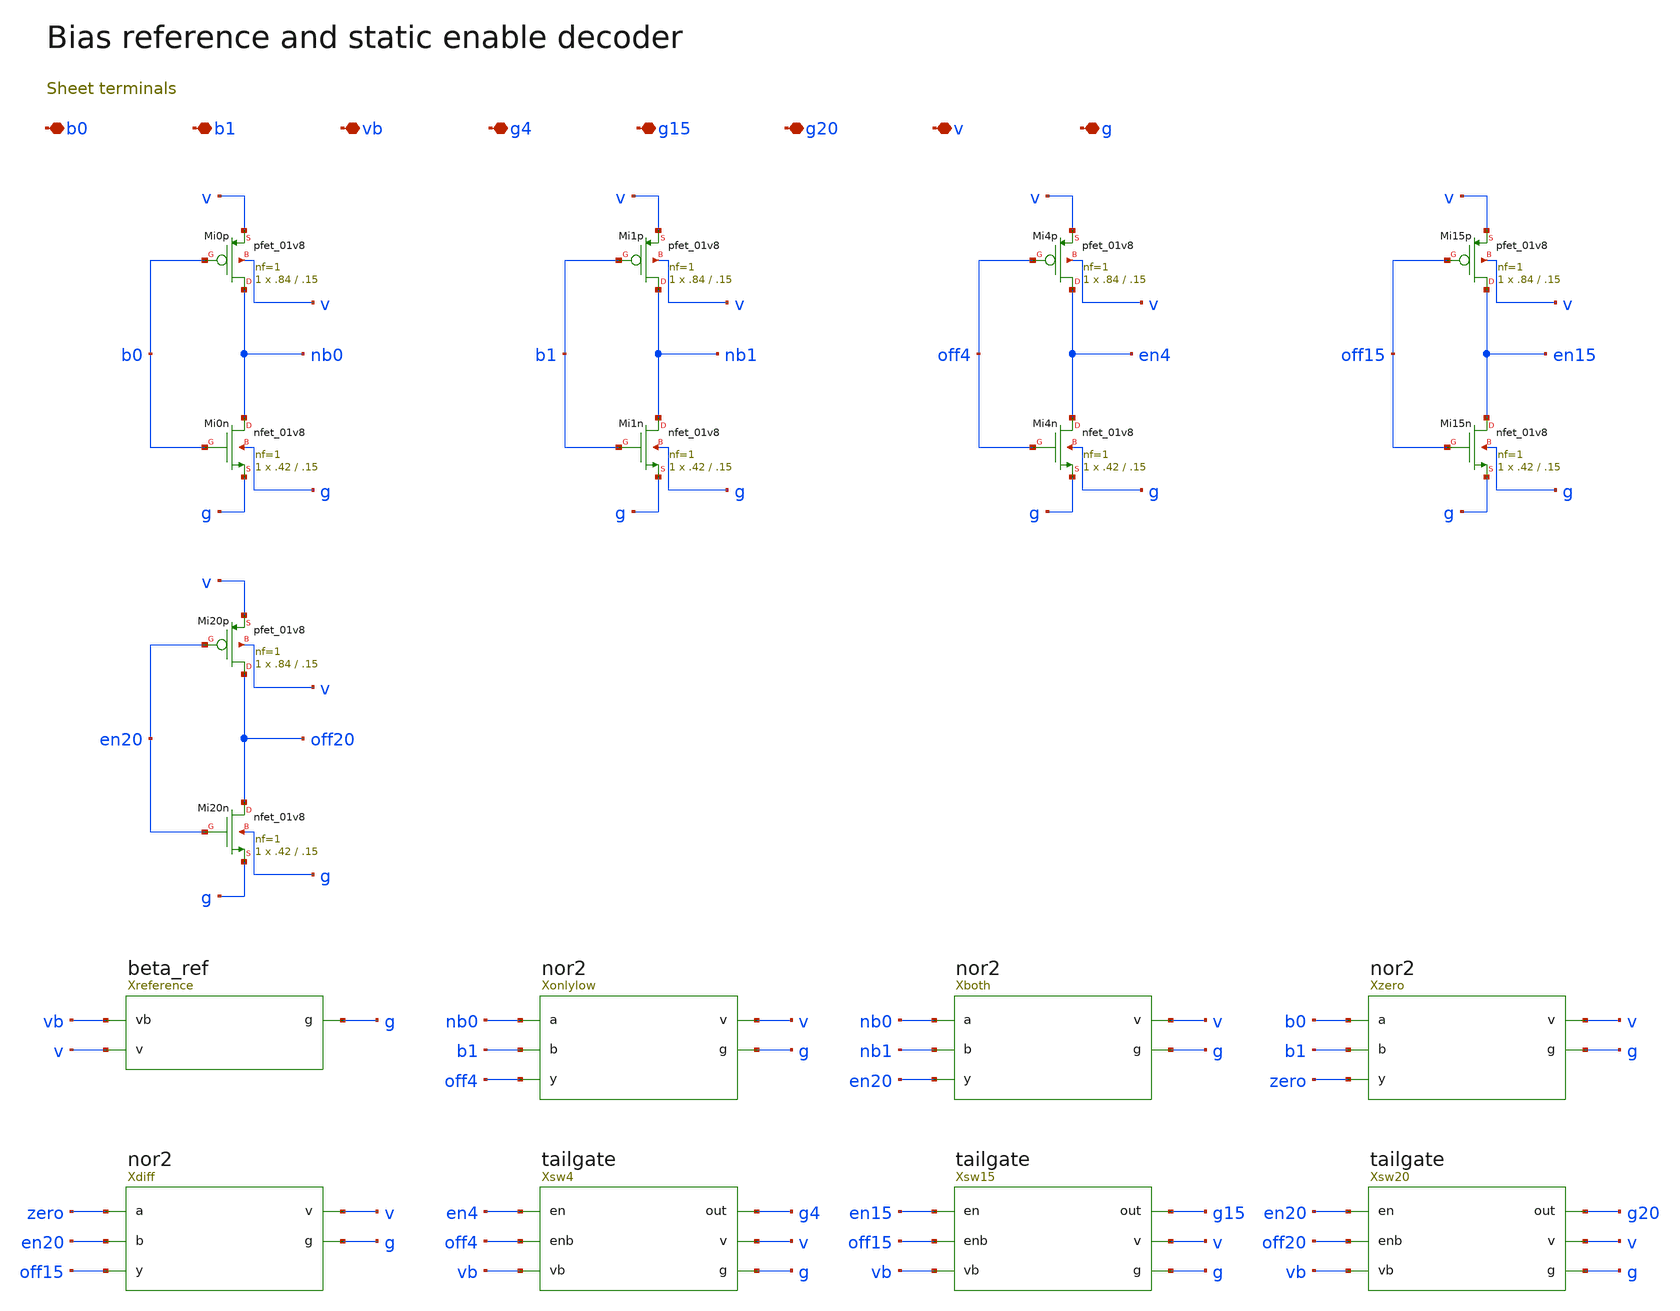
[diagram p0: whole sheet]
** sch_path: review/xschem/bias.sch
**.subckt bias b0 b1 vb g4 g15 g20 v g
*.iopin b0
*.iopin b1
*.iopin vb
*.iopin g4
*.iopin g15
*.iopin g20
*.iopin v
*.iopin g
Xreference vb v g beta_ref
XMi0p nb0 b0 v v sky130_fd_pr__pfet_01v8 L=.15 W=.84 nf=1 ad='int((nf+1)/2) * W/nf * 0.29' as='int((nf+2)/2) * W/nf * 0.29'
+ pd='2*int((nf+1)/2) * (W/nf + 0.29)' ps='2*int((nf+2)/2) * (W/nf + 0.29)' nrd='0.29 / W' nrs='0.29 / W'
+ sa=0 sb=0 sd=0 mult=1 m=1
XMi0n nb0 b0 g g sky130_fd_pr__nfet_01v8 L=.15 W=.42 nf=1 ad='int((1 + 1)/2) * .42 / 1 * 0.29' as='int((1 + 2)/2) * .42 / 1 * 0.29'
+ pd='2*int((1 + 1)/2) * (.42 / 1 + 0.29)' ps='2*int((1 + 2)/2) * (.42 / 1 + 0.29)' nrd='0.29 / .42 ' nrs='0.29 / .42 '
+ sa=0 sb=0 sd=0 mult=1 m=1
XMi1p nb1 b1 v v sky130_fd_pr__pfet_01v8 L=.15 W=.84 nf=1 ad='int((nf+1)/2) * W/nf * 0.29' as='int((nf+2)/2) * W/nf * 0.29'
+ pd='2*int((nf+1)/2) * (W/nf + 0.29)' ps='2*int((nf+2)/2) * (W/nf + 0.29)' nrd='0.29 / W' nrs='0.29 / W'
+ sa=0 sb=0 sd=0 mult=1 m=1
XMi1n nb1 b1 g g sky130_fd_pr__nfet_01v8 L=.15 W=.42 nf=1 ad='int((1 + 1)/2) * .42 / 1 * 0.29' as='int((1 + 2)/2) * .42 / 1 * 0.29'
+ pd='2*int((1 + 1)/2) * (.42 / 1 + 0.29)' ps='2*int((1 + 2)/2) * (.42 / 1 + 0.29)' nrd='0.29 / .42 ' nrs='0.29 / .42 '
+ sa=0 sb=0 sd=0 mult=1 m=1
Xonlylow nb0 b1 off4 v g nor2
XMi4p en4 off4 v v sky130_fd_pr__pfet_01v8 L=.15 W=.84 nf=1 ad='int((nf+1)/2) * W/nf * 0.29' as='int((nf+2)/2) * W/nf * 0.29'
+ pd='2*int((nf+1)/2) * (W/nf + 0.29)' ps='2*int((nf+2)/2) * (W/nf + 0.29)' nrd='0.29 / W' nrs='0.29 / W'
+ sa=0 sb=0 sd=0 mult=1 m=1
XMi4n en4 off4 g g sky130_fd_pr__nfet_01v8 L=.15 W=.42 nf=1 ad='int((1 + 1)/2) * .42 / 1 * 0.29' as='int((1 + 2)/2) * .42 / 1 * 0.29'
+ pd='2*int((1 + 1)/2) * (.42 / 1 + 0.29)' ps='2*int((1 + 2)/2) * (.42 / 1 + 0.29)' nrd='0.29 / .42 ' nrs='0.29 / .42 '
+ sa=0 sb=0 sd=0 mult=1 m=1
Xboth nb0 nb1 en20 v g nor2
Xzero b0 b1 zero v g nor2
Xdiff zero en20 off15 v g nor2
XMi15p en15 off15 v v sky130_fd_pr__pfet_01v8 L=.15 W=.84 nf=1 ad='int((nf+1)/2) * W/nf * 0.29' as='int((nf+2)/2) * W/nf * 0.29'
+ pd='2*int((nf+1)/2) * (W/nf + 0.29)' ps='2*int((nf+2)/2) * (W/nf + 0.29)' nrd='0.29 / W' nrs='0.29 / W'
+ sa=0 sb=0 sd=0 mult=1 m=1
XMi15n en15 off15 g g sky130_fd_pr__nfet_01v8 L=.15 W=.42 nf=1 ad='int((1 + 1)/2) * .42 / 1 * 0.29' as='int((1 + 2)/2) * .42 / 1 * 0.29'
+ pd='2*int((1 + 1)/2) * (.42 / 1 + 0.29)' ps='2*int((1 + 2)/2) * (.42 / 1 + 0.29)' nrd='0.29 / .42 ' nrs='0.29 / .42 '
+ sa=0 sb=0 sd=0 mult=1 m=1
XMi20p off20 en20 v v sky130_fd_pr__pfet_01v8 L=.15 W=.84 nf=1 ad='int((nf+1)/2) * W/nf * 0.29' as='int((nf+2)/2) * W/nf * 0.29'
+ pd='2*int((nf+1)/2) * (W/nf + 0.29)' ps='2*int((nf+2)/2) * (W/nf + 0.29)' nrd='0.29 / W' nrs='0.29 / W'
+ sa=0 sb=0 sd=0 mult=1 m=1
XMi20n off20 en20 g g sky130_fd_pr__nfet_01v8 L=.15 W=.42 nf=1 ad='int((1 + 1)/2) * .42 / 1 * 0.29' as='int((1 + 2)/2) * .42 / 1 * 0.29'
+ pd='2*int((1 + 1)/2) * (.42 / 1 + 0.29)' ps='2*int((1 + 2)/2) * (.42 / 1 + 0.29)' nrd='0.29 / .42 ' nrs='0.29 / .42 '
+ sa=0 sb=0 sd=0 mult=1 m=1
Xsw4 en4 off4 vb g4 v g tailgate
Xsw15 en15 off15 vb g15 v g tailgate
Xsw20 en20 off20 vb g20 v g tailgate
**.ends

* expanding   symbol:  beta_ref.sym # of pins=3
** sym_path: review/xschem/beta_ref.sym
** sch_path: review/xschem/beta_ref.sch
.subckt beta_ref vb v g
*.iopin vb
*.iopin v
*.iopin g
XMp0 vb vb v v sky130_fd_pr__pfet_01v8 L=2 W=2 nf=1 ad='int((nf+1)/2) * W/nf * 0.29' as='int((nf+2)/2) * W/nf * 0.29'
+ pd='2*int((nf+1)/2) * (W/nf + 0.29)' ps='2*int((nf+2)/2) * (W/nf + 0.29)' nrd='0.29 / W' nrs='0.29 / W'
+ sa=0 sb=0 sd=0 mult=1 m=1
XMn0 vn vn g g sky130_fd_pr__nfet_01v8 L=2 W=2 nf=1 ad='int((1 + 1)/2) * 2 / 1 * 0.29' as='int((1 + 2)/2) * 2 / 1 * 0.29'
+ pd='2*int((1 + 1)/2) * (2 / 1 + 0.29)' ps='2*int((1 + 2)/2) * (2 / 1 + 0.29)' nrd='0.29 / 2 ' nrs='0.29 / 2 '
+ sa=0 sb=0 sd=0 mult=1 m=1
XMp1 vn vb v v sky130_fd_pr__pfet_01v8 L=2 W=2 nf=1 ad='int((nf+1)/2) * W/nf * 0.29' as='int((nf+2)/2) * W/nf * 0.29'
+ pd='2*int((nf+1)/2) * (W/nf + 0.29)' ps='2*int((nf+2)/2) * (W/nf + 0.29)' nrd='0.29 / W' nrs='0.29 / W'
+ sa=0 sb=0 sd=0 mult=1 m=1
XMn1 vb vn rs g sky130_fd_pr__nfet_01v8 L=2 W=8 nf=1 ad='int((1 + 1)/2) * 8 / 1 * 0.29' as='int((1 + 2)/2) * 8 / 1 * 0.29'
+ pd='2*int((1 + 1)/2) * (8 / 1 + 0.29)' ps='2*int((1 + 2)/2) * (8 / 1 + 0.29)' nrd='0.29 / 8 ' nrs='0.29 / 8 '
+ sa=0 sb=0 sd=0 mult=1 m=1
XRref0 rs refmid g sky130_fd_pr__res_high_po_0p69 L=97.1 mult=1 m=1
XRref1 refmid g g sky130_fd_pr__res_high_po_0p69 L=97.1 mult=1 m=1
XMweak kick g v v sky130_fd_pr__pfet_01v8 L=12 W=.42 nf=1 ad='int((nf+1)/2) * W/nf * 0.29' as='int((nf+2)/2) * W/nf * 0.29'
+ pd='2*int((nf+1)/2) * (W/nf + 0.29)' ps='2*int((nf+2)/2) * (W/nf + 0.29)' nrd='0.29 / W' nrs='0.29 / W'
+ sa=0 sb=0 sd=0 mult=1 m=1
XMsense kick vn g g sky130_fd_pr__nfet_01v8_lvt L=.15 W=5 nf=1 ad='int((1 + 1)/2) * 5 / 1 * 0.29' as='int((1 + 2)/2) * 5 / 1 * 0.29'
+ pd='2*int((1 + 1)/2) * (5 / 1 + 0.29)' ps='2*int((1 + 2)/2) * (5 / 1 + 0.29)' nrd='0.29 / 5 ' nrs='0.29 / 5 '
+ sa=0 sb=0 sd=0 mult=1 m=1
XMkick vb kick g g sky130_fd_pr__nfet_01v8 L=1 W=.5 nf=1 ad='int((1 + 1)/2) * .5 / 1 * 0.29' as='int((1 + 2)/2) * .5 / 1 * 0.29'
+ pd='2*int((1 + 1)/2) * (.5 / 1 + 0.29)' ps='2*int((1 + 2)/2) * (.5 / 1 + 0.29)' nrd='0.29 / .5 ' nrs='0.29 / .5 '
+ sa=0 sb=0 sd=0 mult=1 m=1
.ends


* expanding   symbol:  nor2.sym # of pins=5
** sym_path: review/xschem/nor2.sym
** sch_path: review/xschem/nor2.sch
.subckt nor2 a b y v g
*.iopin a
*.iopin b
*.iopin y
*.iopin v
*.iopin g
XMp0 mid a v v sky130_fd_pr__pfet_01v8 L=.15 W=.84 nf=1 ad='int((nf+1)/2) * W/nf * 0.29' as='int((nf+2)/2) * W/nf * 0.29'
+ pd='2*int((nf+1)/2) * (W/nf + 0.29)' ps='2*int((nf+2)/2) * (W/nf + 0.29)' nrd='0.29 / W' nrs='0.29 / W'
+ sa=0 sb=0 sd=0 mult=1 m=1
XMp1 y b mid v sky130_fd_pr__pfet_01v8 L=.15 W=.84 nf=1 ad='int((nf+1)/2) * W/nf * 0.29' as='int((nf+2)/2) * W/nf * 0.29'
+ pd='2*int((nf+1)/2) * (W/nf + 0.29)' ps='2*int((nf+2)/2) * (W/nf + 0.29)' nrd='0.29 / W' nrs='0.29 / W'
+ sa=0 sb=0 sd=0 mult=1 m=1
XMn0 y a g g sky130_fd_pr__nfet_01v8 L=.15 W=.42 nf=1 ad='int((1 + 1)/2) * .42 / 1 * 0.29' as='int((1 + 2)/2) * .42 / 1 * 0.29'
+ pd='2*int((1 + 1)/2) * (.42 / 1 + 0.29)' ps='2*int((1 + 2)/2) * (.42 / 1 + 0.29)' nrd='0.29 / .42 ' nrs='0.29 / .42 '
+ sa=0 sb=0 sd=0 mult=1 m=1
XMn1 y b g g sky130_fd_pr__nfet_01v8 L=.15 W=.42 nf=1 ad='int((1 + 1)/2) * .42 / 1 * 0.29' as='int((1 + 2)/2) * .42 / 1 * 0.29'
+ pd='2*int((1 + 1)/2) * (.42 / 1 + 0.29)' ps='2*int((1 + 2)/2) * (.42 / 1 + 0.29)' nrd='0.29 / .42 ' nrs='0.29 / .42 '
+ sa=0 sb=0 sd=0 mult=1 m=1
.ends


* expanding   symbol:  tailgate.sym # of pins=6
** sym_path: review/xschem/tailgate.sym
** sch_path: review/xschem/tailgate.sch
.subckt tailgate en enb vb out v g
*.iopin en
*.iopin enb
*.iopin vb
*.iopin out
*.iopin v
*.iopin g
XMonp out enb vb v sky130_fd_pr__pfet_01v8 L=.15 W=.84 nf=1 ad='int((nf+1)/2) * W/nf * 0.29' as='int((nf+2)/2) * W/nf * 0.29'
+ pd='2*int((nf+1)/2) * (W/nf + 0.29)' ps='2*int((nf+2)/2) * (W/nf + 0.29)' nrd='0.29 / W' nrs='0.29 / W'
+ sa=0 sb=0 sd=0 mult=1 m=1
XMonn out en vb g sky130_fd_pr__nfet_01v8 L=.15 W=.42 nf=1 ad='int((1 + 1)/2) * .42 / 1 * 0.29' as='int((1 + 2)/2) * .42 / 1 * 0.29'
+ pd='2*int((1 + 1)/2) * (.42 / 1 + 0.29)' ps='2*int((1 + 2)/2) * (.42 / 1 + 0.29)' nrd='0.29 / .42 ' nrs='0.29 / .42 '
+ sa=0 sb=0 sd=0 mult=1 m=1
XMoff out en v v sky130_fd_pr__pfet_01v8 L=.15 W=.84 nf=1 ad='int((nf+1)/2) * W/nf * 0.29' as='int((nf+2)/2) * W/nf * 0.29'
+ pd='2*int((nf+1)/2) * (W/nf + 0.29)' ps='2*int((nf+2)/2) * (W/nf + 0.29)' nrd='0.29 / W' nrs='0.29 / W'
+ sa=0 sb=0 sd=0 mult=1 m=1
.ends

.end
